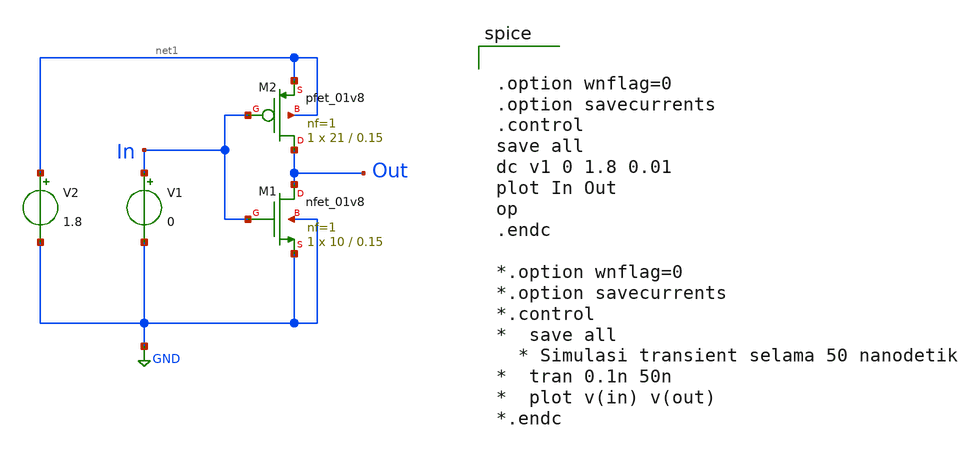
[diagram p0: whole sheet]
** sch_path: sch/duta_cmos_inv.sch
**.subckt duta_cmos_inv
XM1 Out In GND GND sky130_fd_pr__nfet_01v8 L=0.15 W=10 nf=1 ad='int((1 + 1)/2) * 10 / 1 * 0.29' as='int((1 + 2)/2) * 10 / 1 * 0.29'
+ pd='2*int((1 + 1)/2) * (10 / 1 + 0.29)' ps='2*int((1 + 2)/2) * (10 / 1 + 0.29)' nrd='0.29 / 10 ' nrs='0.29 / 10 '
+ sa=0 sb=0 sd=0 mult=1 m=1
XM2 Out In net1 net1 sky130_fd_pr__pfet_01v8 L=0.15 W=21 nf=1 ad='int((1 + 1)/2) * 21 / 1 * 0.29' as='int((1 + 2)/2) * 21 / 1 * 0.29'
+ pd='2*int((1 + 1)/2) * (21 / 1 + 0.29)' ps='2*int((1 + 2)/2) * (21 / 1 + 0.29)' nrd='0.29 / 21 ' nrs='0.29 / 21 '
+ sa=0 sb=0 sd=0 mult=1 m=1
V1 In GND 0
V2 net1 GND 1.8
**** begin user architecture code


.lib /foss/pdks/sky130A/libs.tech/ngspice/sky130.lib.spice tt

.param mc_mm_switch=0
.param mc_pr_switch=1




.option wnflag=0
.option savecurrents
.control
save all
dc v1 0 1.8 0.01
plot In Out
op
.endc

*.option wnflag=0
*.option savecurrents
*.control
*  save all
  * Simulasi transient selama 50 nanodetik
*  tran 0.1n 50n
*  plot v(in) v(out)
*.endc


**** end user architecture code
**.ends
.GLOBAL GND
.end
